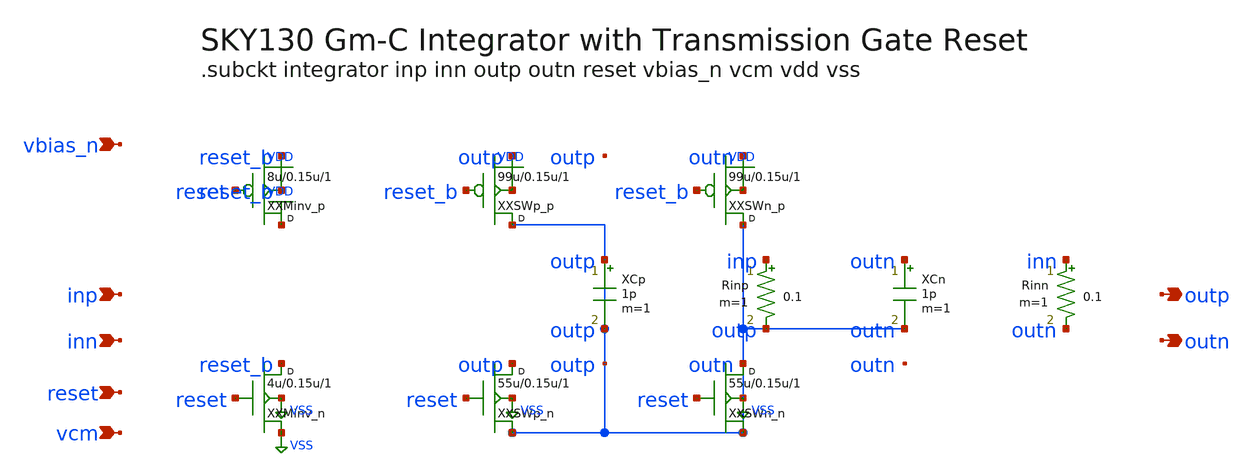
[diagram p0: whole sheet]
** sch_path: data/sch/ode_integrator.sch
**.subckt ode_integrator inp inn reset vbias_n vcm outp outn
*.ipin inp
*.ipin inn
*.ipin reset
*.ipin vbias_n
*.ipin vcm
*.opin outp
*.opin outn
XXMinv_n reset_b reset VSS VSS sky130_fd_pr__nfet_01v8 w=4u l=0.15u m=1
XXMinv_p VDD reset reset_b VDD sky130_fd_pr__pfet_01v8 w=8u l=0.15u m=1
XCp VSS VSS 1p m=1
XXSWp_n outp reset VSS VSS sky130_fd_pr__nfet_01v8_lvt w=55u l=0.15u m=1
XXSWp_p VSS reset_b outp VDD sky130_fd_pr__pfet_01v8 w=99u l=0.15u m=1
XCn outn VSS 1p m=1
XXSWn_n VSS reset VSS VSS sky130_fd_pr__nfet_01v8_lvt w=55u l=0.15u m=1
XXSWn_p VSS reset_b outn VDD sky130_fd_pr__pfet_01v8 w=99u l=0.15u m=1
Rinp inp VSS 0.1 m=1
Rinn inn outn 0.1 m=1
**.ends
.GLOBAL VSS
.GLOBAL VDD
.end
